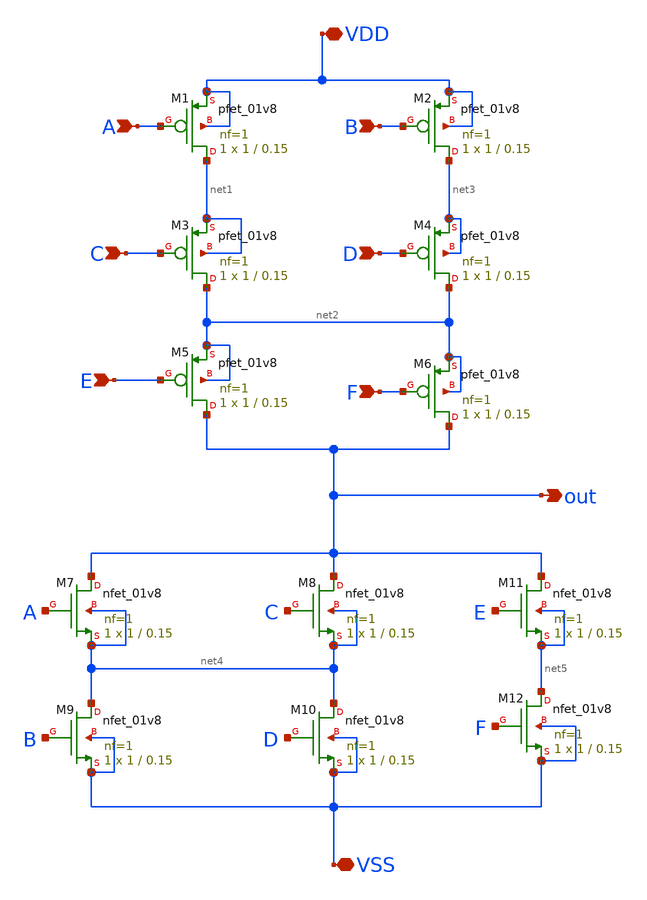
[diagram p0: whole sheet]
** sch_path: week2/Fn/Fn_prelayout.sch
**.subckt Fn_prelayout A B C D E F out VDD VSS
*.ipin A
*.ipin B
*.ipin C
*.ipin D
*.ipin E
*.ipin F
*.opin out
*.iopin VDD
*.iopin VSS
XM1 net1 A VDD VDD sky130_fd_pr__pfet_01v8 L=0.15 W=1 nf=1 ad='int((nf+1)/2) * W/nf * 0.29' as='int((nf+2)/2) * W/nf * 0.29'
+ pd='2*int((nf+1)/2) * (W/nf + 0.29)' ps='2*int((nf+2)/2) * (W/nf + 0.29)' nrd='0.29 / W' nrs='0.29 / W'
+ sa=0 sb=0 sd=0 mult=1 m=1
XM2 net3 B VDD VDD sky130_fd_pr__pfet_01v8 L=0.15 W=1 nf=1 ad='int((nf+1)/2) * W/nf * 0.29' as='int((nf+2)/2) * W/nf * 0.29'
+ pd='2*int((nf+1)/2) * (W/nf + 0.29)' ps='2*int((nf+2)/2) * (W/nf + 0.29)' nrd='0.29 / W' nrs='0.29 / W'
+ sa=0 sb=0 sd=0 mult=1 m=1
XM3 net2 C net1 net1 sky130_fd_pr__pfet_01v8 L=0.15 W=1 nf=1 ad='int((nf+1)/2) * W/nf * 0.29' as='int((nf+2)/2) * W/nf * 0.29'
+ pd='2*int((nf+1)/2) * (W/nf + 0.29)' ps='2*int((nf+2)/2) * (W/nf + 0.29)' nrd='0.29 / W' nrs='0.29 / W'
+ sa=0 sb=0 sd=0 mult=1 m=1
XM4 net2 D net3 net3 sky130_fd_pr__pfet_01v8 L=0.15 W=1 nf=1 ad='int((nf+1)/2) * W/nf * 0.29' as='int((nf+2)/2) * W/nf * 0.29'
+ pd='2*int((nf+1)/2) * (W/nf + 0.29)' ps='2*int((nf+2)/2) * (W/nf + 0.29)' nrd='0.29 / W' nrs='0.29 / W'
+ sa=0 sb=0 sd=0 mult=1 m=1
XM5 out E net2 net2 sky130_fd_pr__pfet_01v8 L=0.15 W=1 nf=1 ad='int((nf+1)/2) * W/nf * 0.29' as='int((nf+2)/2) * W/nf * 0.29'
+ pd='2*int((nf+1)/2) * (W/nf + 0.29)' ps='2*int((nf+2)/2) * (W/nf + 0.29)' nrd='0.29 / W' nrs='0.29 / W'
+ sa=0 sb=0 sd=0 mult=1 m=1
XM6 out F net2 net2 sky130_fd_pr__pfet_01v8 L=0.15 W=1 nf=1 ad='int((nf+1)/2) * W/nf * 0.29' as='int((nf+2)/2) * W/nf * 0.29'
+ pd='2*int((nf+1)/2) * (W/nf + 0.29)' ps='2*int((nf+2)/2) * (W/nf + 0.29)' nrd='0.29 / W' nrs='0.29 / W'
+ sa=0 sb=0 sd=0 mult=1 m=1
XM7 out A net4 net4 sky130_fd_pr__nfet_01v8 L=0.15 W=1 nf=1 ad='int((nf+1)/2) * W/nf * 0.29' as='int((nf+2)/2) * W/nf * 0.29'
+ pd='2*int((nf+1)/2) * (W/nf + 0.29)' ps='2*int((nf+2)/2) * (W/nf + 0.29)' nrd='0.29 / W' nrs='0.29 / W'
+ sa=0 sb=0 sd=0 mult=1 m=1
XM8 out C net4 net4 sky130_fd_pr__nfet_01v8 L=0.15 W=1 nf=1 ad='int((nf+1)/2) * W/nf * 0.29' as='int((nf+2)/2) * W/nf * 0.29'
+ pd='2*int((nf+1)/2) * (W/nf + 0.29)' ps='2*int((nf+2)/2) * (W/nf + 0.29)' nrd='0.29 / W' nrs='0.29 / W'
+ sa=0 sb=0 sd=0 mult=1 m=1
XM9 net4 B VSS VSS sky130_fd_pr__nfet_01v8 L=0.15 W=1 nf=1 ad='int((nf+1)/2) * W/nf * 0.29' as='int((nf+2)/2) * W/nf * 0.29'
+ pd='2*int((nf+1)/2) * (W/nf + 0.29)' ps='2*int((nf+2)/2) * (W/nf + 0.29)' nrd='0.29 / W' nrs='0.29 / W'
+ sa=0 sb=0 sd=0 mult=1 m=1
XM10 net4 D VSS VSS sky130_fd_pr__nfet_01v8 L=0.15 W=1 nf=1 ad='int((nf+1)/2) * W/nf * 0.29' as='int((nf+2)/2) * W/nf * 0.29'
+ pd='2*int((nf+1)/2) * (W/nf + 0.29)' ps='2*int((nf+2)/2) * (W/nf + 0.29)' nrd='0.29 / W' nrs='0.29 / W'
+ sa=0 sb=0 sd=0 mult=1 m=1
XM11 out E net5 net5 sky130_fd_pr__nfet_01v8 L=0.15 W=1 nf=1 ad='int((nf+1)/2) * W/nf * 0.29' as='int((nf+2)/2) * W/nf * 0.29'
+ pd='2*int((nf+1)/2) * (W/nf + 0.29)' ps='2*int((nf+2)/2) * (W/nf + 0.29)' nrd='0.29 / W' nrs='0.29 / W'
+ sa=0 sb=0 sd=0 mult=1 m=1
XM12 net5 F VSS VSS sky130_fd_pr__nfet_01v8 L=0.15 W=1 nf=1 ad='int((nf+1)/2) * W/nf * 0.29' as='int((nf+2)/2) * W/nf * 0.29'
+ pd='2*int((nf+1)/2) * (W/nf + 0.29)' ps='2*int((nf+2)/2) * (W/nf + 0.29)' nrd='0.29 / W' nrs='0.29 / W'
+ sa=0 sb=0 sd=0 mult=1 m=1
**.ends
.end
